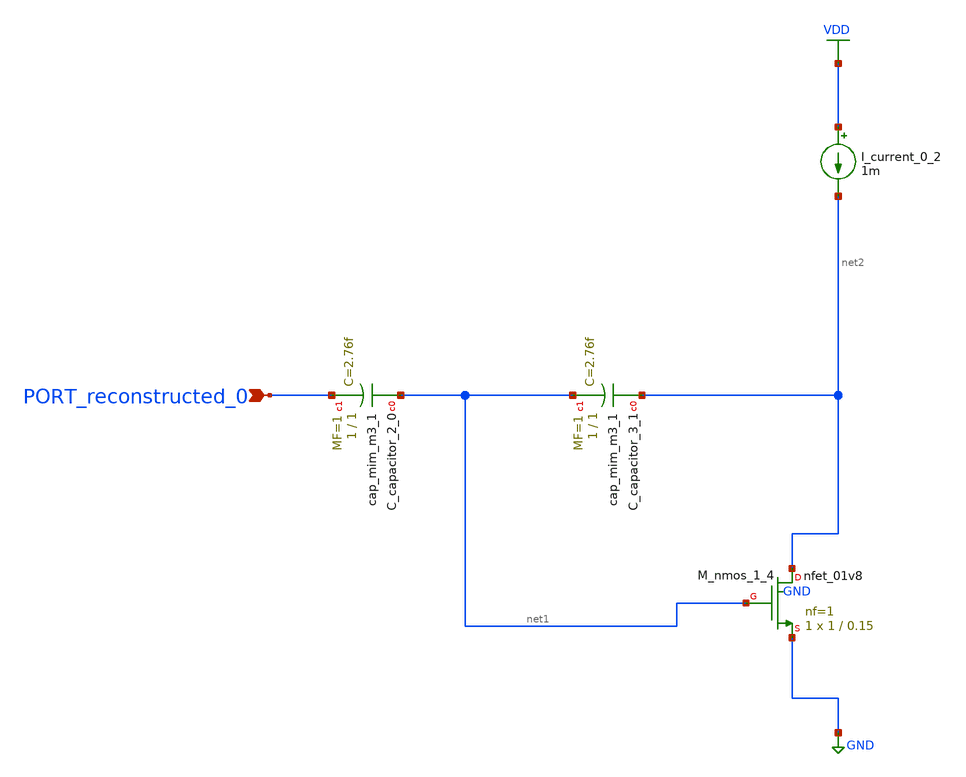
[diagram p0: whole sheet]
** sch_path: schematics/AMSNet/406.sch
**.subckt 406 PORT_reconstructed_0
*.ipin PORT_reconstructed_0
XC_capacitor_2_0 net1 PORT_reconstructed_0 sky130_fd_pr__cap_mim_m3_1 W=1 L=1 MF=1 m=1
XC_capacitor_3_1 net2 net1 sky130_fd_pr__cap_mim_m3_1 W=1 L=1 MF=1 m=1
I_current_0_2 VDD net2 1m
XM_nmos_1_4 net2 net1 GND GND sky130_fd_pr__nfet_01v8 L=0.15 W=1 nf=1 ad='int((1 + 1)/2) * 1 / 1 * 0.29'
+ as='int((1 + 2)/2) * 1 / 1 * 0.29' pd='2*int((1 + 1)/2) * (1 / 1 + 0.29)' ps='2*int((1 + 2)/2) * (1 / 1 + 0.29)'
+ nrd='0.29 / 1 ' nrs='0.29 / 1 ' sa=0 sb=0 sd=0 mult=1 m=1
**.ends
.GLOBAL GND
.GLOBAL VDD
.end
